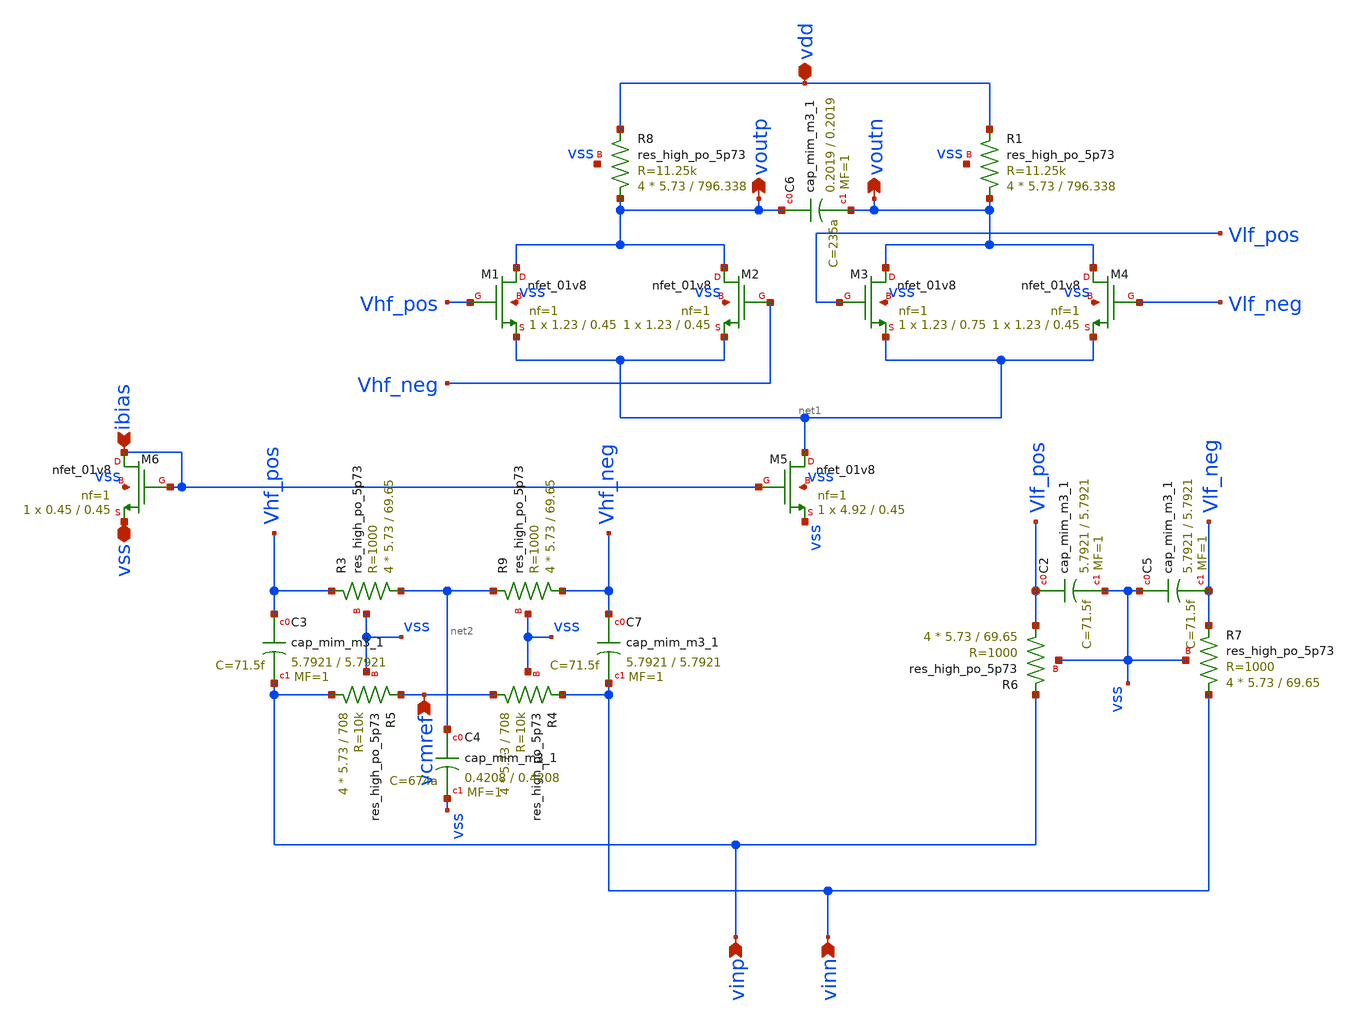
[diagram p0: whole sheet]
** sch_path: CTLE/filterred_power_detector_sizing.sch
**.subckt filterred_power_detector_sizing vinp vinn voutp voutn ibias vss vdd vcmref
*.ipin vinp
*.ipin vinn
*.opin voutp
*.opin voutn
*.ipin ibias
*.iopin vss
*.iopin vdd
*.ipin vcmref
XM1 voutp Vhf_pos net1 vss sky130_fd_pr__nfet_01v8 L=0.45 W=1.23 nf=1 ad='int((nf+1)/2) * W/nf * 0.29'
+ as='int((nf+2)/2) * W/nf * 0.29' pd='2*int((nf+1)/2) * (W/nf + 0.29)' ps='2*int((nf+2)/2) * (W/nf + 0.29)'
+ nrd='0.29 / W' nrs='0.29 / W' sa=0 sb=0 sd=0 mult=1 m=1
XM2 voutp Vhf_neg net1 vss sky130_fd_pr__nfet_01v8 L=0.45 W=1.23 nf=1 ad='int((nf+1)/2) * W/nf * 0.29'
+ as='int((nf+2)/2) * W/nf * 0.29' pd='2*int((nf+1)/2) * (W/nf + 0.29)' ps='2*int((nf+2)/2) * (W/nf + 0.29)'
+ nrd='0.29 / W' nrs='0.29 / W' sa=0 sb=0 sd=0 mult=1 m=1
XM3 voutn Vlf_pos net1 vss sky130_fd_pr__nfet_01v8 L=0.75 W=1.23 nf=1 ad='int((nf+1)/2) * W/nf * 0.29'
+ as='int((nf+2)/2) * W/nf * 0.29' pd='2*int((nf+1)/2) * (W/nf + 0.29)' ps='2*int((nf+2)/2) * (W/nf + 0.29)'
+ nrd='0.29 / W' nrs='0.29 / W' sa=0 sb=0 sd=0 mult=1 m=1
XM4 voutn Vlf_neg net1 vss sky130_fd_pr__nfet_01v8 L=0.45 W=1.23 nf=1 ad='int((nf+1)/2) * W/nf * 0.29'
+ as='int((nf+2)/2) * W/nf * 0.29' pd='2*int((nf+1)/2) * (W/nf + 0.29)' ps='2*int((nf+2)/2) * (W/nf + 0.29)'
+ nrd='0.29 / W' nrs='0.29 / W' sa=0 sb=0 sd=0 mult=1 m=1
XC7 Vhf_neg vinn sky130_fd_pr__cap_mim_m3_1 W=5.7921 L=5.7921 MF=1 m=1
XC3 Vhf_pos vinp sky130_fd_pr__cap_mim_m3_1 W=5.7921 L=5.7921 MF=1 m=1
XR9 Vhf_neg net2 vss sky130_fd_pr__res_high_po_5p73 L=69.65 mult=4 m=4
XR3 net2 Vhf_pos vss sky130_fd_pr__res_high_po_5p73 L=69.65 mult=4 m=4
XR4 vcmref vinn vss sky130_fd_pr__res_high_po_5p73 L=708 mult=4 m=4
XR5 vinp vcmref vss sky130_fd_pr__res_high_po_5p73 L=708 mult=4 m=4
XC4 net2 vss sky130_fd_pr__cap_mim_m3_1 W=0.4208 L=0.4208 MF=1 m=1
XR6 Vlf_pos vinp vss sky130_fd_pr__res_high_po_5p73 L=69.65 mult=4 m=4
XR7 vinn Vlf_neg vss sky130_fd_pr__res_high_po_5p73 L=69.65 mult=4 m=4
XC2 Vlf_pos vss sky130_fd_pr__cap_mim_m3_1 W=5.7921 L=5.7921 MF=1 m=1
XC5 vss Vlf_neg sky130_fd_pr__cap_mim_m3_1 W=5.7921 L=5.7921 MF=1 m=1
XC6 voutp voutn sky130_fd_pr__cap_mim_m3_1 W=0.2019 L=0.2019 MF=1 m=1
XR8 voutp vdd vss sky130_fd_pr__res_high_po_5p73 L=796.338 mult=4 m=4
XR1 voutn vdd vss sky130_fd_pr__res_high_po_5p73 L=796.338 mult=4 m=4
XM5 net1 ibias vss vss sky130_fd_pr__nfet_01v8 L=0.45 W=4.92 nf=1 ad='int((nf+1)/2) * W/nf * 0.29' as='int((nf+2)/2) * W/nf * 0.29'
+ pd='2*int((nf+1)/2) * (W/nf + 0.29)' ps='2*int((nf+2)/2) * (W/nf + 0.29)' nrd='0.29 / W' nrs='0.29 / W'
+ sa=0 sb=0 sd=0 mult=1 m=1
XM6 ibias ibias vss vss sky130_fd_pr__nfet_01v8 L=0.45 W=0.45 nf=1 ad='int((nf+1)/2) * W/nf * 0.29' as='int((nf+2)/2) * W/nf * 0.29'
+ pd='2*int((nf+1)/2) * (W/nf + 0.29)' ps='2*int((nf+2)/2) * (W/nf + 0.29)' nrd='0.29 / W' nrs='0.29 / W'
+ sa=0 sb=0 sd=0 mult=1 m=1
**.ends
.end
